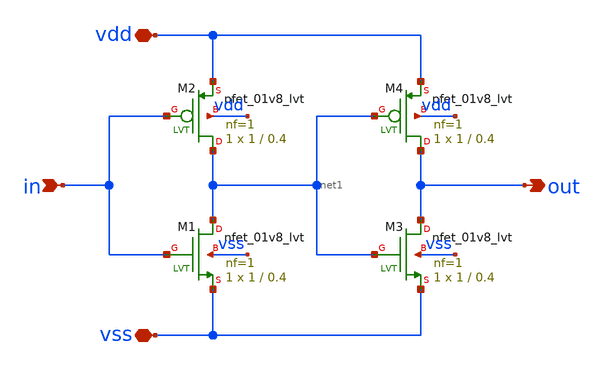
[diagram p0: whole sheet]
** sch_path: xschem/logic/buffer_lvt.sch
**.subckt buffer_lvt vdd vss in out
*.iopin vdd
*.iopin vss
*.ipin in
*.opin out
XM1 net1 in vss vss sky130_fd_pr__nfet_01v8_lvt L=0.4 W=1 nf=1 ad='int((nf+1)/2) * W/nf * 0.29' as='int((nf+2)/2) * W/nf * 0.29'
+ pd='2*int((nf+1)/2) * (W/nf + 0.29)' ps='2*int((nf+2)/2) * (W/nf + 0.29)' nrd='0.29 / W' nrs='0.29 / W'
+ sa=0 sb=0 sd=0 mult=1 m=1
XM2 net1 in vdd vdd sky130_fd_pr__pfet_01v8_lvt L=0.4 W=1 nf=1 ad='int((nf+1)/2) * W/nf * 0.29' as='int((nf+2)/2) * W/nf * 0.29'
+ pd='2*int((nf+1)/2) * (W/nf + 0.29)' ps='2*int((nf+2)/2) * (W/nf + 0.29)' nrd='0.29 / W' nrs='0.29 / W'
+ sa=0 sb=0 sd=0 mult=1 m=1
XM3 out net1 vss vss sky130_fd_pr__nfet_01v8_lvt L=0.4 W=1 nf=1 ad='int((nf+1)/2) * W/nf * 0.29' as='int((nf+2)/2) * W/nf * 0.29'
+ pd='2*int((nf+1)/2) * (W/nf + 0.29)' ps='2*int((nf+2)/2) * (W/nf + 0.29)' nrd='0.29 / W' nrs='0.29 / W'
+ sa=0 sb=0 sd=0 mult=1 m=1
XM4 out net1 vdd vdd sky130_fd_pr__pfet_01v8_lvt L=0.4 W=1 nf=1 ad='int((nf+1)/2) * W/nf * 0.29' as='int((nf+2)/2) * W/nf * 0.29'
+ pd='2*int((nf+1)/2) * (W/nf + 0.29)' ps='2*int((nf+2)/2) * (W/nf + 0.29)' nrd='0.29 / W' nrs='0.29 / W'
+ sa=0 sb=0 sd=0 mult=1 m=1
**.ends
.end
